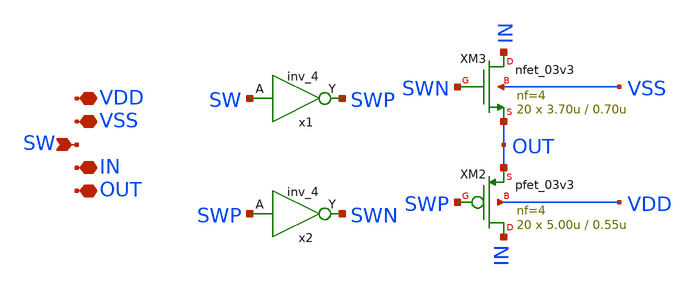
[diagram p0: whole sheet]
** sch_path: designs/libs/core_switch-matrix/trans-gate/trans-gate.sch
**.subckt trans-gate VDD VSS IN OUT SW
*.iopin VDD
*.iopin VSS
*.iopin IN
*.iopin OUT
*.ipin SW
XM3 IN SWN OUT VSS nfet_03v3 L=0.70u W=3.70u nf=4 ad='int((nf+1)/2) * W/nf * 0.18u' as='int((nf+2)/2) * W/nf * 0.18u'
+ pd='2*int((nf+1)/2) * (W/nf + 0.18u)' ps='2*int((nf+2)/2) * (W/nf + 0.18u)' nrd='0.18u / W' nrs='0.18u / W'
+ sa=0 sb=0 sd=0 m=20
XM2 IN SWP OUT VDD pfet_03v3 L=0.55u W=5.00u nf=4 ad='int((nf+1)/2) * W/nf * 0.18u' as='int((nf+2)/2) * W/nf * 0.18u'
+ pd='2*int((nf+1)/2) * (W/nf + 0.18u)' ps='2*int((nf+2)/2) * (W/nf + 0.18u)' nrd='0.18u / W' nrs='0.18u / W'
+ sa=0 sb=0 sd=0 m=20
x1 SW VSSd VDDd VSSd VDDd SWP gf180mcu_fd_sc_mcu9t5v0__inv_4
x2 SWP VSSd VDDd VSSd VDDd SWN gf180mcu_fd_sc_mcu9t5v0__inv_4
**.ends
.end
